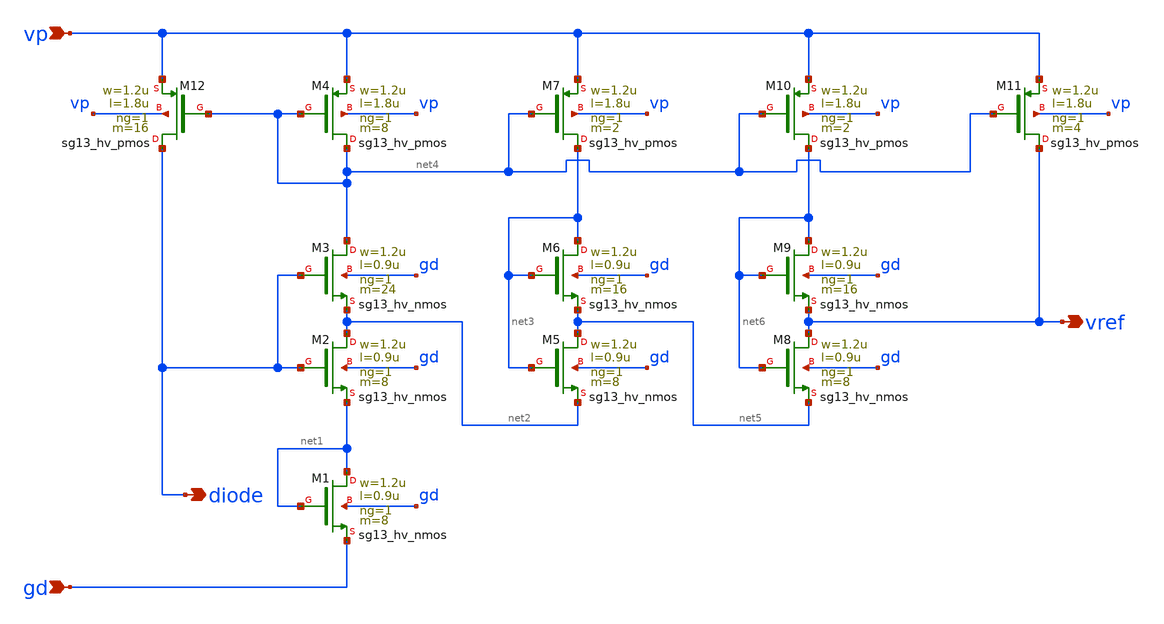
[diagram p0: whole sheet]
** sch_path: circuit/bandgap_selfbias_core.sch
**.subckt bandgap_selfbias_core diode gd vp vref
*.opin diode
*.ipin gd
*.ipin vp
*.opin vref
XM1 net1 net1 gd gd sg13_hv_nmos w=1.2u l=0.9u ng=1 m=8 mm_ok=1
XM2 net2 diode net1 gd sg13_hv_nmos w=1.2u l=0.9u ng=1 m=8 mm_ok=1
XM3 net4 diode net2 gd sg13_hv_nmos w=1.2u l=0.9u ng=1 m=24 mm_ok=1
XM4 net4 net4 vp vp sg13_hv_pmos w=1.2u l=1.8u ng=1 m=8 mm_ok=1
XM5 net5 net3 net2 gd sg13_hv_nmos w=1.2u l=0.9u ng=1 m=8 mm_ok=1
XM6 net3 net3 net5 gd sg13_hv_nmos w=1.2u l=0.9u ng=1 m=16 mm_ok=1
XM7 net3 net4 vp vp sg13_hv_pmos w=1.2u l=1.8u ng=1 m=2 mm_ok=1
XM8 vref net6 net5 gd sg13_hv_nmos w=1.2u l=0.9u ng=1 m=8 mm_ok=1
XM9 net6 net6 vref gd sg13_hv_nmos w=1.2u l=0.9u ng=1 m=16 mm_ok=1
XM10 net6 net4 vp vp sg13_hv_pmos w=1.2u l=1.8u ng=1 m=2 mm_ok=1
XM11 vref net4 vp vp sg13_hv_pmos w=1.2u l=1.8u ng=1 m=4 mm_ok=1
XM12 diode net4 vp vp sg13_hv_pmos w=1.2u l=1.8u ng=1 m=16 mm_ok=1
**.ends
.end
